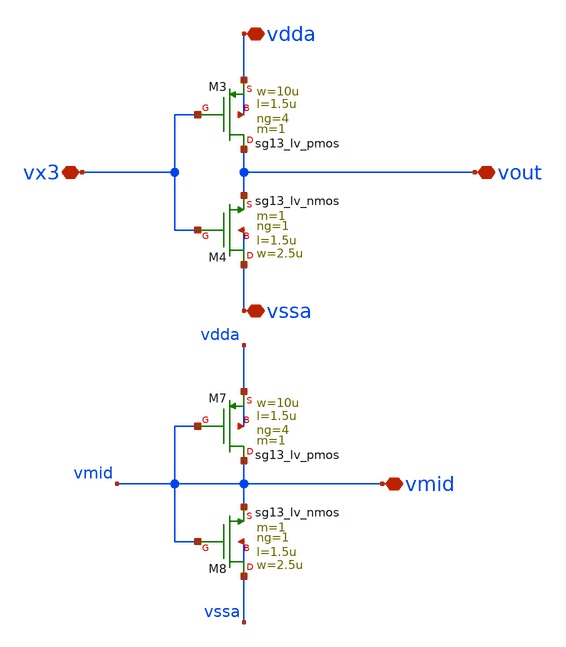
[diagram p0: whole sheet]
** sch_path: 5_Design/4_Layout/Team 5/splitUpSimulationsAndSchematics/integ_5_split3.sch
**.subckt integ_5_split3 vssa vdda vmid vout vx3
*.iopin vssa
*.iopin vdda
*.iopin vmid
*.iopin vout
*.iopin vx3
XM3 vout vx3 vdda vdda sg13_lv_pmos w=10u l=1.5u ng=4 m=1 mm_ok=1
XM4 vssa vx3 vout vssa sg13_lv_nmos w=2.5u l=1.5u ng=1 m=1 mm_ok=1
XM7 vmid vmid vdda vdda sg13_lv_pmos w=10u l=1.5u ng=4 m=1 mm_ok=1
XM8 vssa vmid vmid vssa sg13_lv_nmos w=2.5u l=1.5u ng=1 m=1 mm_ok=1
**.ends
.end
